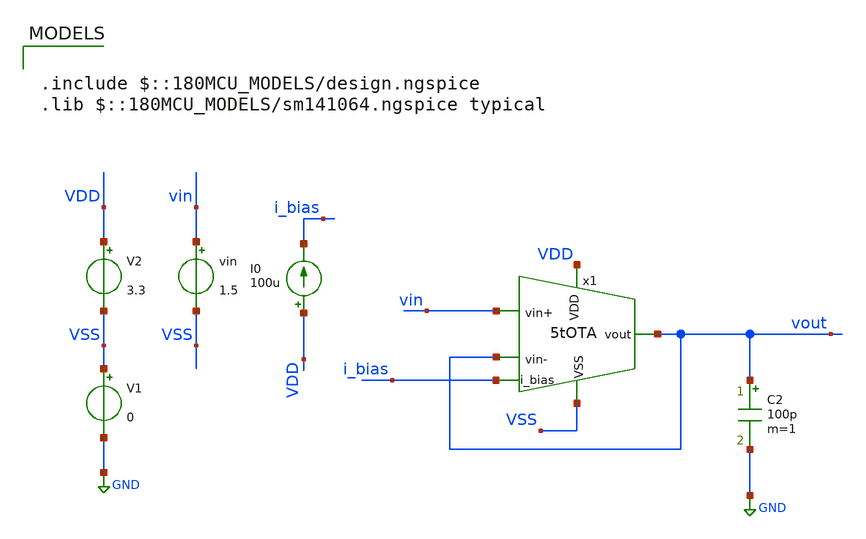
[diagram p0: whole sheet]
** sch_path: designs/libs/core_amps/ota_5t/5tOTA_tb2.sch
**.subckt 5tOTA_tb2
V1 VSS GND 0
V2 VDD VSS 3.3
I0 VDD i_bias 100u
vin vin VSS 1.5
C2 vout GND 100p m=1
x1 VDD vout vin vout i_bias VSS 5tOTA
**** begin user architecture code

.include $::180MCU_MODELS/design.ngspice
.lib $::180MCU_MODELS/sm141064.ngspice typical



.control
op
show all

show m.x1.xm1.m0 m.x1.xm2.m0 m.x1.xm3.m0 m.x1.xm4.m0 m.x1.xm5.m0 m.x1.xm6.m0 : gm id vdsat vds

print @m.x1.xm4.m0[gm]
let gm4 = @m.x1.xm4.m0[gm]
let id4 = @m.x1.xm4.m0[id]
print gm4/id4
print @m.x1.xm4.m0[id]

let gm1 = @m.x1.xm1.m0[gm]
let id1 = @m.x1.xm1.m0[id]
print gm1/id1

let gm2 = @m.x1.xm2.m0[gm]
let id2 = @m.x1.xm2.m0[id]
print gm2/id2

let gm3 = @m.x1.xm3.m0[gm]
let id3 = @m.x1.xm3.m0[id]
print gm3/id3

let gm4 = @m.x1.xm1.m0[gm]
let id4 = @m.x1.xm1.m0[id]
print gm4/id4

let gm5 = @m.x1.xm1.m0[gm]
let id5 = @m.x1.xm1.m0[id]
print gm5/id5

let gm6 = @m.x1.xm1.m0[gm]
let id6 = @m.x1.xm1.m0[id]
print gm6/id6

let vsat1 = @m.x1.xm1.m0[vdsat]
print vsat1

let vsat2 = @m.x1.xm2.m0[vdsat]
print vsat2

let vsat3 = @m.x1.xm3.m0[vdsat]
print vsat3

let vsat4 = @m.x1.xm4.m0[vdsat]
print vsat4

let vsat5 = @m.x1.xm5.m0[vdsat]
print vsat5

let vsat6 = @m.x1.xm6.m0[vdsat]
print vsat6

print v(vout)

*DC Unity
dc vin 0 4 0.001
let gain = deriv(v(vout))
meas dc icmr_low when gain = 0.95 rise = 1
meas dc icmr_high when gain = 0.95 fall = 1
let swing_low = icmr_low
let swing_high = icmr_high
print icmr_low icmr_high
print swing_high - swing_low
plot v(vout) gain

.endc


**** end user architecture code
**.ends

* expanding   symbol:  libs/core_amps/ota_5t/5tOTA.sym # of pins=6
** sym_path: designs/5tOTA.sym
** sch_path: designs/5tOTA.sch
.subckt 5tOTA VDD vout vin+ vin- i_bias VSS
*.ipin VDD
*.opin vout
*.ipin i_bias
*.ipin vin+
*.ipin vin-
*.ipin VSS
XM1 net1 vin+ net2 VSS nfet_03v3 L=0.5u W=11.43u nf=1 ad='int((nf+1)/2) * W/nf * 0.18u' as='int((nf+2)/2) * W/nf * 0.18u'
+ pd='2*int((nf+1)/2) * (W/nf + 0.18u)' ps='2*int((nf+2)/2) * (W/nf + 0.18u)' nrd='0.18u / W' nrs='0.18u / W'
+ sa=0 sb=0 sd=0 m=1
XM2 vout vin- net2 VSS nfet_03v3 L=0.5u W=11.43u nf=1 ad='int((nf+1)/2) * W/nf * 0.18u' as='int((nf+2)/2) * W/nf * 0.18u'
+ pd='2*int((nf+1)/2) * (W/nf + 0.18u)' ps='2*int((nf+2)/2) * (W/nf + 0.18u)' nrd='0.18u / W' nrs='0.18u / W'
+ sa=0 sb=0 sd=0 m=1
XM3 net1 net1 VDD VDD pfet_03v3 L=0.5u W=22.86u nf=1 ad='int((nf+1)/2) * W/nf * 0.18u' as='int((nf+2)/2) * W/nf * 0.18u'
+ pd='2*int((nf+1)/2) * (W/nf + 0.18u)' ps='2*int((nf+2)/2) * (W/nf + 0.18u)' nrd='0.18u / W' nrs='0.18u / W'
+ sa=0 sb=0 sd=0 m=1
XM4 vout net1 VDD VDD pfet_03v3 L=0.5u W=22.86u nf=1 ad='int((nf+1)/2) * W/nf * 0.18u' as='int((nf+2)/2) * W/nf * 0.18u'
+ pd='2*int((nf+1)/2) * (W/nf + 0.18u)' ps='2*int((nf+2)/2) * (W/nf + 0.18u)' nrd='0.18u / W' nrs='0.18u / W'
+ sa=0 sb=0 sd=0 m=1
XM5 net2 i_bias VSS VSS nfet_03v3 L=0.5u W=22.86u nf=1 ad='int((nf+1)/2) * W/nf * 0.18u' as='int((nf+2)/2) * W/nf * 0.18u'
+ pd='2*int((nf+1)/2) * (W/nf + 0.18u)' ps='2*int((nf+2)/2) * (W/nf + 0.18u)' nrd='0.18u / W' nrs='0.18u / W'
+ sa=0 sb=0 sd=0 m=1
XM6 i_bias i_bias VSS VSS nfet_03v3 L=0.5u W=22.86u nf=1 ad='int((nf+1)/2) * W/nf * 0.18u' as='int((nf+2)/2) * W/nf * 0.18u'
+ pd='2*int((nf+1)/2) * (W/nf + 0.18u)' ps='2*int((nf+2)/2) * (W/nf + 0.18u)' nrd='0.18u / W' nrs='0.18u / W'
+ sa=0 sb=0 sd=0 m=1
.ends

.GLOBAL GND
.end
